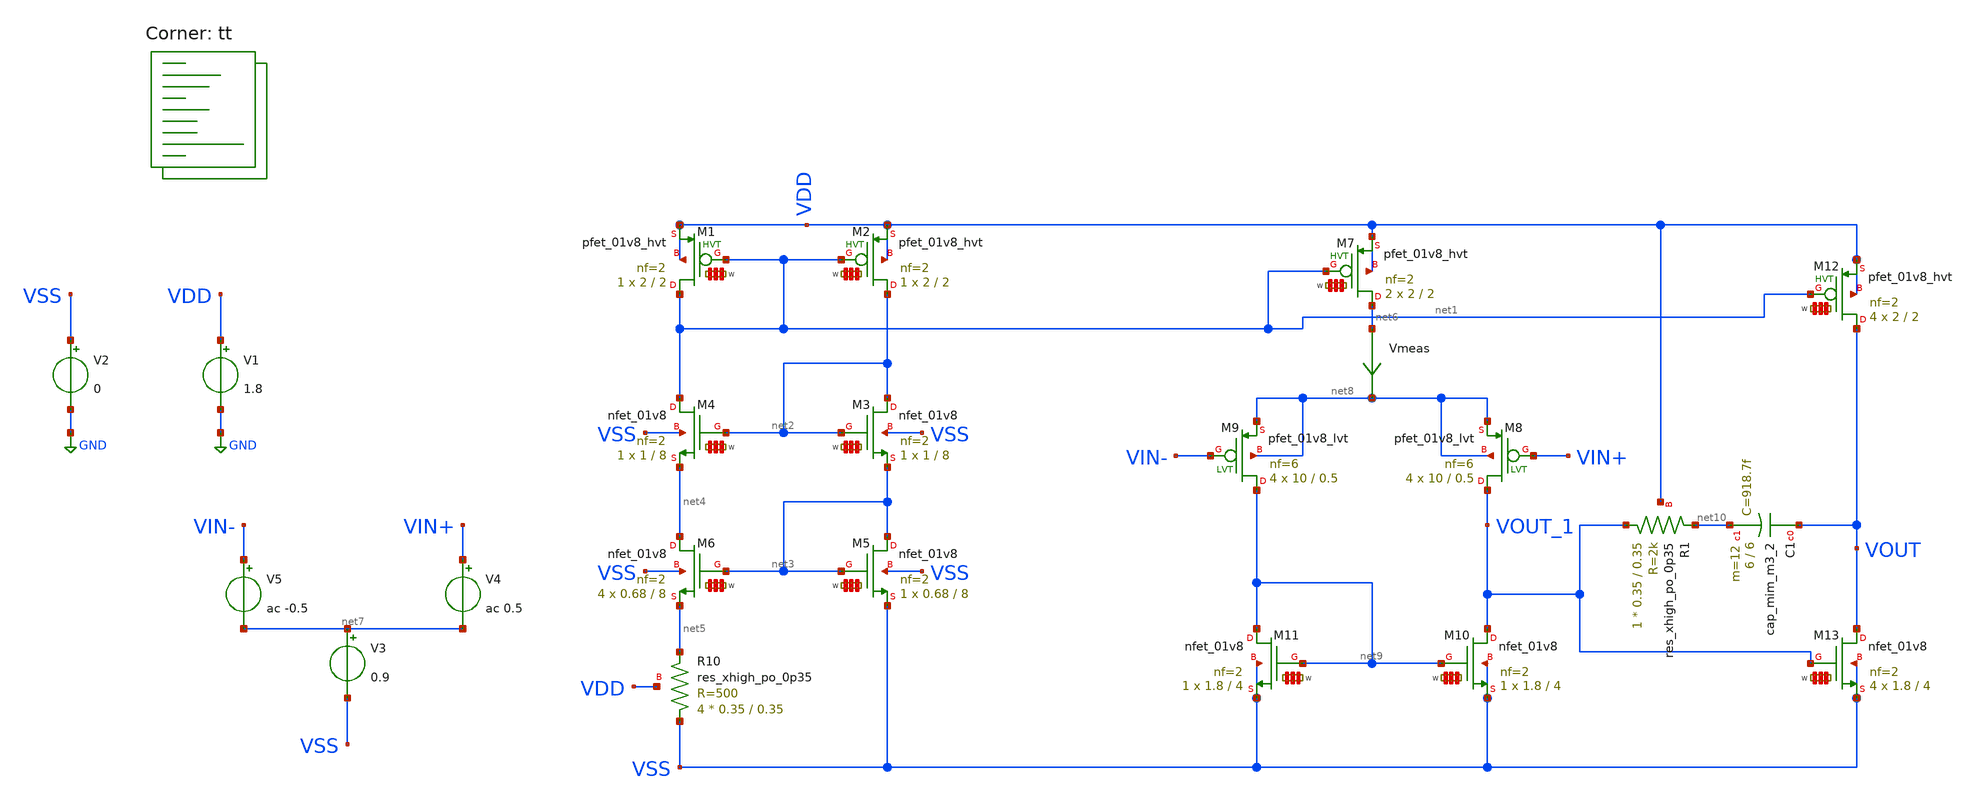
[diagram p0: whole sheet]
** sch_path: my_ip/sky130A/2_stage_op_amp_sky130/testbench.sch
**.subckt testbench
V1 VDD GND 1.8
V2 VSS GND 0
XM5 net3 net3 VSS VSS sky130_fd_pr__nfet_01v8 L=8 W='0.68 * 2 ' nf=2 ad='int((2 + 1)/2) * 0.68 / 2 * 0.29'
+ as='int((2 + 2)/2) * 0.68 / 2 * 0.29' pd='2*int((2 + 1)/2) * (0.68 / 2 + 0.29)' ps='2*int((2 + 2)/2) * (0.68 / 2 + 0.29)'
+ nrd='0.29 / 0.68 ' nrs='0.29 / 0.68 ' sa=0 sb=0 sd=0 mult=1 m=1
XM6 net4 net3 net5 VSS sky130_fd_pr__nfet_01v8 L=8 W='0.68 * 2 ' nf=2 ad='int((2 + 1)/2) * 0.68 / 2 * 0.29'
+ as='int((2 + 2)/2) * 0.68 / 2 * 0.29' pd='2*int((2 + 1)/2) * (0.68 / 2 + 0.29)' ps='2*int((2 + 2)/2) * (0.68 / 2 + 0.29)'
+ nrd='0.29 / 0.68 ' nrs='0.29 / 0.68 ' sa=0 sb=0 sd=0 mult=4 m=4
Vmeas net6 net8 0
.save i(vmeas)
XM7 net6 net1 VDD VDD sky130_fd_pr__pfet_01v8_hvt L=2 W='2 * 2 ' nf=2 ad='int((2 + 1)/2) * 2 / 2 * 0.29'
+ as='int((2 + 2)/2) * 2 / 2 * 0.29' pd='2*int((2 + 1)/2) * (2 / 2 + 0.29)' ps='2*int((2 + 2)/2) * (2 / 2 + 0.29)'
+ nrd='0.29 / 2 ' nrs='0.29 / 2 ' sa=0 sb=0 sd=0 mult=2 m=2
V3 net7 VSS 0.9
XM2 net2 net1 VDD VDD sky130_fd_pr__pfet_01v8_hvt L=2 W='2 * 2 ' nf=2 ad='int((2 + 1)/2) * 2 / 2 * 0.29'
+ as='int((2 + 2)/2) * 2 / 2 * 0.29' pd='2*int((2 + 1)/2) * (2 / 2 + 0.29)' ps='2*int((2 + 2)/2) * (2 / 2 + 0.29)'
+ nrd='0.29 / 2 ' nrs='0.29 / 2 ' sa=0 sb=0 sd=0 mult=1 m=1
XM1 net1 net1 VDD VDD sky130_fd_pr__pfet_01v8_hvt L=2 W='2 * 2 ' nf=2 ad='int((2 + 1)/2) * 2 / 2 * 0.29'
+ as='int((2 + 2)/2) * 2 / 2 * 0.29' pd='2*int((2 + 1)/2) * (2 / 2 + 0.29)' ps='2*int((2 + 2)/2) * (2 / 2 + 0.29)'
+ nrd='0.29 / 2 ' nrs='0.29 / 2 ' sa=0 sb=0 sd=0 mult=1 m=1
XR10 VSS net5 VDD sky130_fd_pr__res_xhigh_po_0p35 L=0.35 mult=4 m=4
XM4 net1 net2 net4 VSS sky130_fd_pr__nfet_01v8 L=8 W='1 * 2 ' nf=2 ad='int((2 + 1)/2) * 1 / 2 * 0.29'
+ as='int((2 + 2)/2) * 1 / 2 * 0.29' pd='2*int((2 + 1)/2) * (1 / 2 + 0.29)' ps='2*int((2 + 2)/2) * (1 / 2 + 0.29)'
+ nrd='0.29 / 1 ' nrs='0.29 / 1 ' sa=0 sb=0 sd=0 mult=1 m=1
XM3 net2 net2 net3 VSS sky130_fd_pr__nfet_01v8 L=8 W='1 * 2 ' nf=2 ad='int((2 + 1)/2) * 1 / 2 * 0.29'
+ as='int((2 + 2)/2) * 1 / 2 * 0.29' pd='2*int((2 + 1)/2) * (1 / 2 + 0.29)' ps='2*int((2 + 2)/2) * (1 / 2 + 0.29)'
+ nrd='0.29 / 1 ' nrs='0.29 / 1 ' sa=0 sb=0 sd=0 mult=1 m=1
V4 VIN+ net7 ac 0.5
V5 VIN- net7 ac -0.5
XM8 VOUT_1 VIN+ net8 net8 sky130_fd_pr__pfet_01v8_lvt L=0.5 W=10 nf=6 ad='int((6 + 1)/2) * 10 / 6 * 0.29'
+ as='int((6 + 2)/2) * 10 / 6 * 0.29' pd='2*int((6 + 1)/2) * (10 / 6 + 0.29)' ps='2*int((6 + 2)/2) * (10 / 6 + 0.29)'
+ nrd='0.29 / 10 ' nrs='0.29 / 10 ' sa=0 sb=0 sd=0 mult=4 m=4
XM9 net9 VIN- net8 net8 sky130_fd_pr__pfet_01v8_lvt L=0.5 W=10 nf=6 ad='int((6 + 1)/2) * 10 / 6 * 0.29'
+ as='int((6 + 2)/2) * 10 / 6 * 0.29' pd='2*int((6 + 1)/2) * (10 / 6 + 0.29)' ps='2*int((6 + 2)/2) * (10 / 6 + 0.29)'
+ nrd='0.29 / 10 ' nrs='0.29 / 10 ' sa=0 sb=0 sd=0 mult=4 m=4
XM10 VOUT_1 net9 VSS VSS sky130_fd_pr__nfet_01v8 L=4 W='1.8 * 2 ' nf=2 ad='int((2 + 1)/2) * 1.8 / 2 * 0.29'
+ as='int((2 + 2)/2) * 1.8 / 2 * 0.29' pd='2*int((2 + 1)/2) * (1.8 / 2 + 0.29)' ps='2*int((2 + 2)/2) * (1.8 / 2 + 0.29)'
+ nrd='0.29 / 1.8 ' nrs='0.29 / 1.8 ' sa=0 sb=0 sd=0 mult=1 m=1
XM11 net9 net9 VSS VSS sky130_fd_pr__nfet_01v8 L=4 W='1.8 * 2 ' nf=2 ad='int((2 + 1)/2) * 1.8 / 2 * 0.29'
+ as='int((2 + 2)/2) * 1.8 / 2 * 0.29' pd='2*int((2 + 1)/2) * (1.8 / 2 + 0.29)' ps='2*int((2 + 2)/2) * (1.8 / 2 + 0.29)'
+ nrd='0.29 / 1.8 ' nrs='0.29 / 1.8 ' sa=0 sb=0 sd=0 mult=1 m=1
XM12 VOUT net1 VDD VDD sky130_fd_pr__pfet_01v8_hvt L=2 W='2 * 2 ' nf=2 ad='int((2 + 1)/2) * 2 / 2 * 0.29'
+ as='int((2 + 2)/2) * 2 / 2 * 0.29' pd='2*int((2 + 1)/2) * (2 / 2 + 0.29)' ps='2*int((2 + 2)/2) * (2 / 2 + 0.29)'
+ nrd='0.29 / 2 ' nrs='0.29 / 2 ' sa=0 sb=0 sd=0 mult=4 m=4
XM13 VOUT VOUT_1 VSS VSS sky130_fd_pr__nfet_01v8 L=4 W='1.8 * 2 ' nf=2 ad='int((2 + 1)/2) * 1.8 / 2 * 0.29'
+ as='int((2 + 2)/2) * 1.8 / 2 * 0.29' pd='2*int((2 + 1)/2) * (1.8 / 2 + 0.29)' ps='2*int((2 + 2)/2) * (1.8 / 2 + 0.29)'
+ nrd='0.29 / 1.8 ' nrs='0.29 / 1.8 ' sa=0 sb=0 sd=0 mult=4 m=4
XC1 VOUT net10 sky130_fd_pr__cap_mim_m3_2 W=6 L=6 MF=12 m=12
XR1 VOUT_1 net10 VDD sky130_fd_pr__res_xhigh_po_0p35 L=0.35 mult=1 m=1
**** begin user architecture code
.lib $::SKYWATER_MODELS/sky130.lib.spice tt

**************************************************************
**************************************************************
**************************************************************
**************************************************************
**************************************************************
*LIBs*********************************************************
**************************************************************
**************************************************************
**************************************************************
**************************************************************
**************************************************************
*.lib $::SKYWATER_MODELS/sky130.lib.spice tt
* chose the corners in the corner file
* tt_mm for mismatch
* ss ff sf fs standart corners
* ll hh lh hl capacitor and resistors corners
* mc for total process variation including corners
**************************************************************
**************************************************************
**************************************************************
**************************************************************
**************************************************************
*Corners/montecarlo options***********************************
**************************************************************
**************************************************************
**************************************************************
**************************************************************
**************************************************************
.TEMP 27
**************************************************************
**************************************************************
**************************************************************
**************************************************************
*SIMULATION and Plots*****************************************
**************************************************************
**************************************************************
**************************************************************
**************************************************************
.control
save all
dc V3 0 1.8 0.001
*dc simulation
plot i(Vmeas)
plot v(VOUT_1)
plot v(VOUT)
ac dec 10 1 50G
plot db(v(VOUT)) (180*ph(v(VOUT))/pi)
.endc

**** end user architecture code
**.ends
.GLOBAL GND
.end
